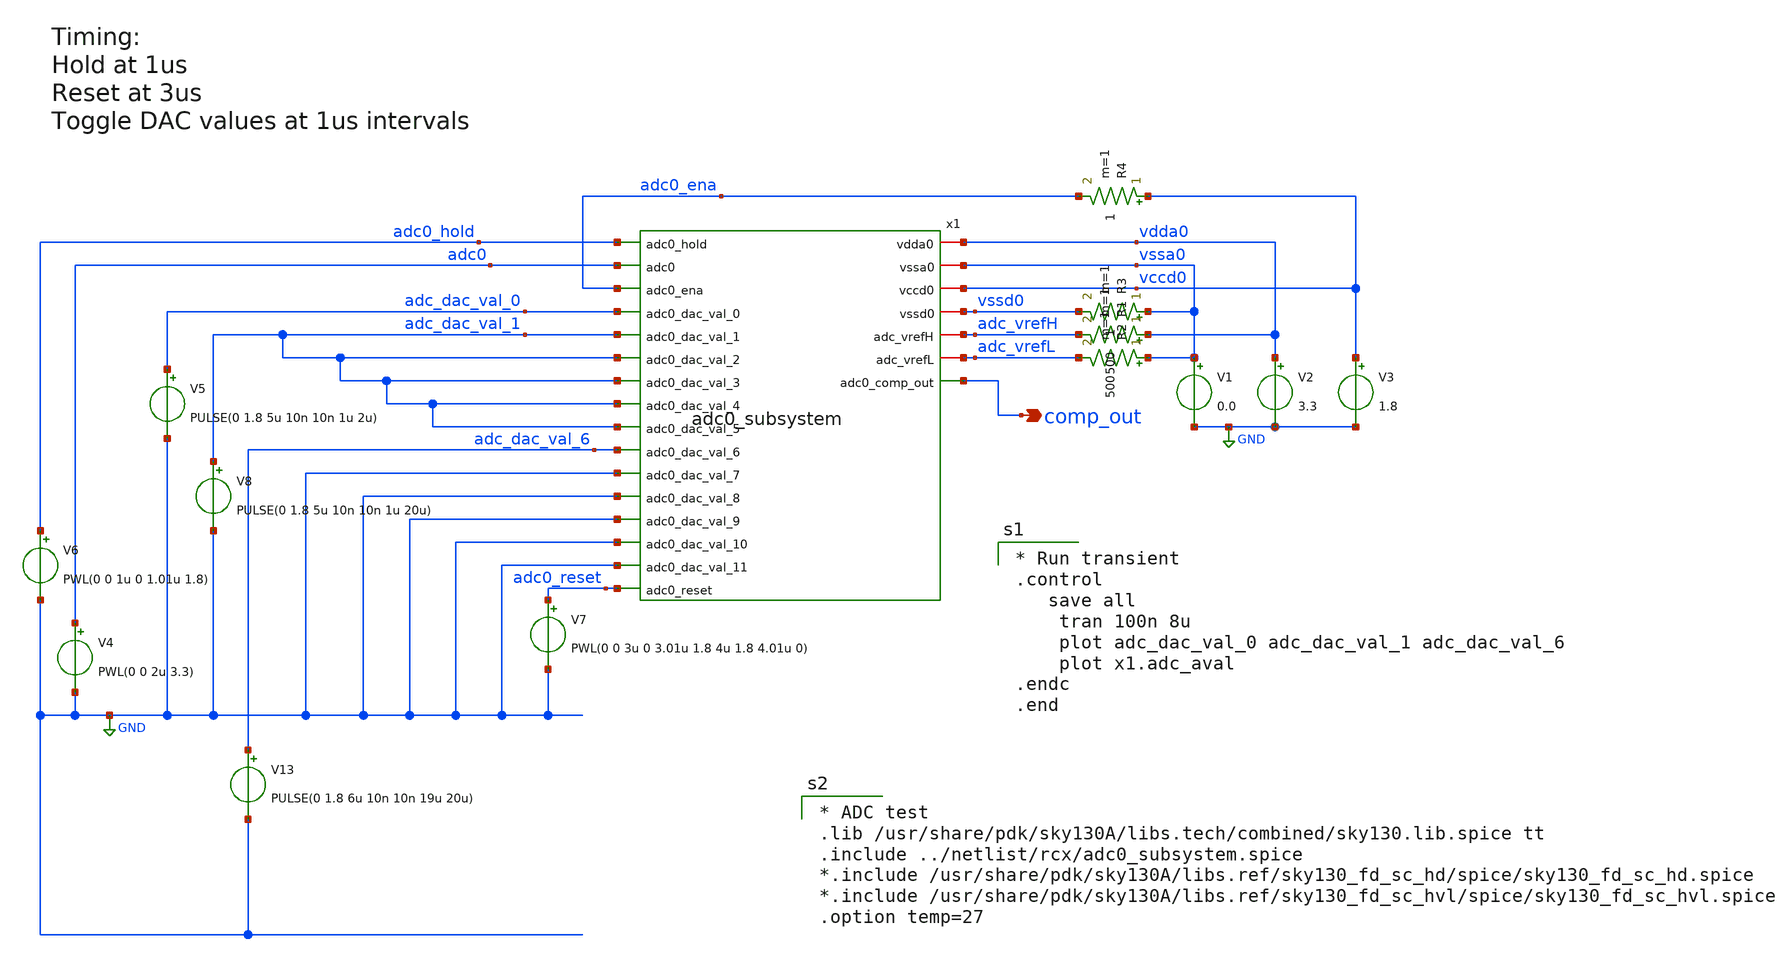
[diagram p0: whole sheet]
** sch_path: cace/adc_calibration_tb2.sch
**.subckt adc_calibration_tb2 comp_out
*.opin comp_out
x1 vdda0 vssa0 vccd0 vssd0 adc_vrefH adc_vrefL adc0_hold adc0 adc0_ena adc_dac_val_0 adc_dac_val_1
+ adc_dac_val_1 adc_dac_val_1 comp_out adc_dac_val_1 adc_dac_val_1 adc_dac_val_6 GND GND GND GND GND adc0_reset
+ adc0_subsystem
V1 vssa0 GND 0.0
V2 vdda0 GND 3.3
V3 vccd0 GND 1.8
V4 adc0 GND PWL(0 0 2u 3.3)
V5 adc_dac_val_0 GND PULSE(0 1.8 5u 10n 10n 1u 2u)
V6 adc0_hold GND PWL(0 0 1u 0 1.01u 1.8)
V7 adc0_reset GND PWL(0 0 3u 0 3.01u 1.8 4u 1.8 4.01u 0)
V13 adc_dac_val_6 GND PULSE(0 1.8 6u 10n 10n 19u 20u)
R1 vdda0 adc_vrefH 500 m=1
R2 vssa0 adc_vrefL 500 m=1
R3 vssa0 vssd0 1 m=1
R4 vccd0 adc0_ena 1 m=1
V8 adc_dac_val_1 GND PULSE(0 1.8 5u 10n 10n 1u 20u)
**** begin user architecture code

* Run transient
.control
   save all
    tran 100n 8u
    plot adc_dac_val_0 adc_dac_val_1 adc_dac_val_6
    plot x1.adc_aval
.endc
.end


* ADC test
.lib /usr/share/pdk/sky130A/libs.tech/combined/sky130.lib.spice tt
.include ../netlist/rcx/adc0_subsystem.spice
*.include /usr/share/pdk/sky130A/libs.ref/sky130_fd_sc_hd/spice/sky130_fd_sc_hd.spice
*.include /usr/share/pdk/sky130A/libs.ref/sky130_fd_sc_hvl/spice/sky130_fd_sc_hvl.spice
.option temp=27

**** end user architecture code
**.ends
.GLOBAL GND
.end
